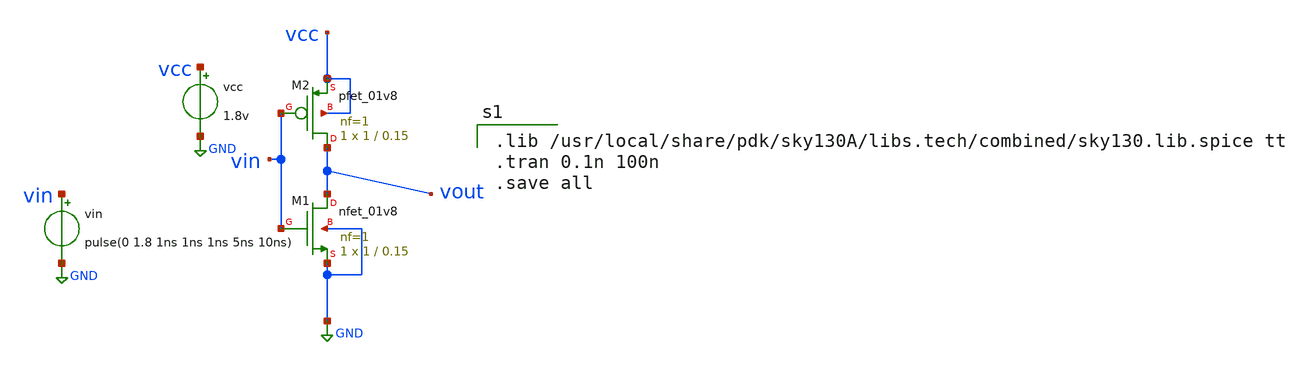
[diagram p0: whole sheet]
** sch_path: Circuit Files/circuits/first_test/untitled.sch
**.subckt untitled
vin vin GND pulse(0 1.8 1ns 1ns 1ns 5ns 10ns)
vcc vcc GND 1.8v
XM1 vout vin GND GND sky130_fd_pr__nfet_01v8 L=0.15 W=1 nf=1 ad='int((nf+1)/2) * W/nf * 0.29' as='int((nf+2)/2) * W/nf * 0.29'
+ pd='2*int((nf+1)/2) * (W/nf + 0.29)' ps='2*int((nf+2)/2) * (W/nf + 0.29)' nrd='0.29 / W' nrs='0.29 / W'
+ sa=0 sb=0 sd=0 mult=1 m=1
XM2 vout vin vcc vcc sky130_fd_pr__pfet_01v8 L=0.15 W=1 nf=1 ad='int((nf+1)/2) * W/nf * 0.29' as='int((nf+2)/2) * W/nf * 0.29'
+ pd='2*int((nf+1)/2) * (W/nf + 0.29)' ps='2*int((nf+2)/2) * (W/nf + 0.29)' nrd='0.29 / W' nrs='0.29 / W'
+ sa=0 sb=0 sd=0 mult=1 m=1
**** begin user architecture code

.lib /usr/local/share/pdk/sky130A/libs.tech/combined/sky130.lib.spice tt
.tran 0.1n 100n
.save all

**** end user architecture code
**.ends
.GLOBAL GND
.end
